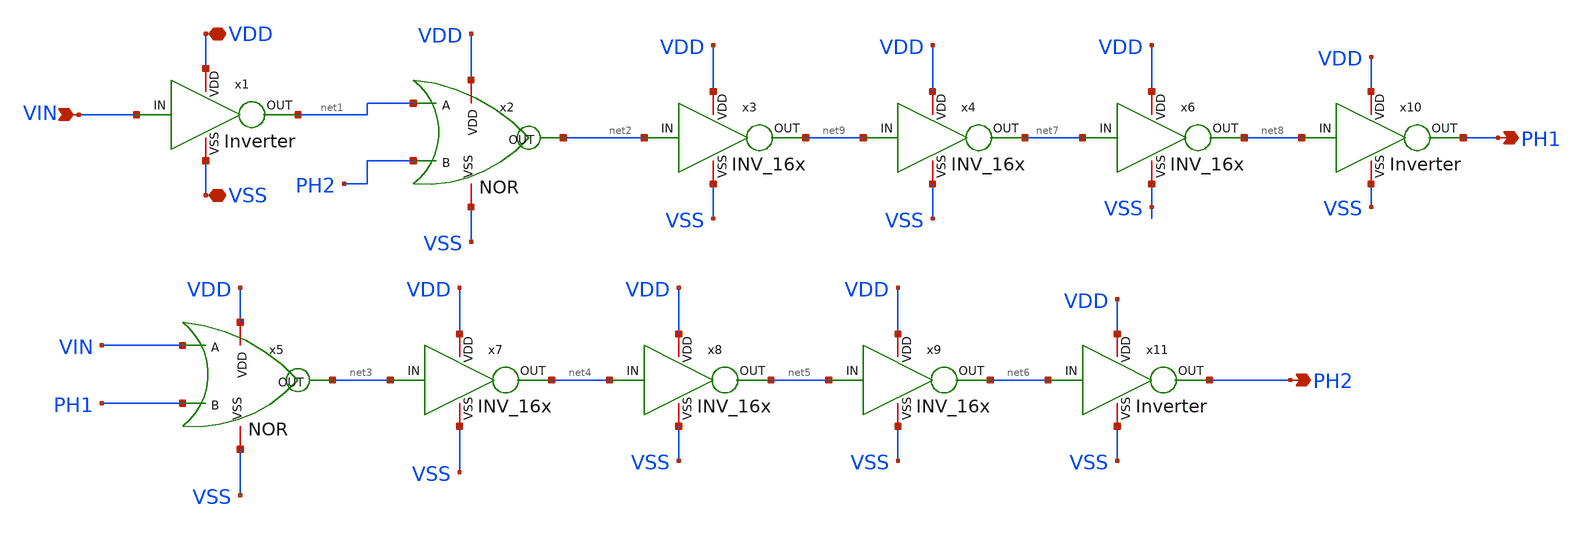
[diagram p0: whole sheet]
** sch_path: SCOP_INPUT_AND_MUX_PAKISTAN_03/Xschem/Non_OvL_CLK_Gen/Non_Overlapping_clk.sch
**.subckt Non_Overlapping_clk VDD VSS VIN PH1 PH2
*.iopin VDD
*.iopin VSS
*.ipin VIN
*.opin PH1
*.opin PH2
x1 VDD net1 VIN VSS Inverter
x10 VDD PH1 net8 VSS Inverter
x11 VDD PH2 net6 VSS Inverter
x3 VDD net9 net2 VSS INV_16x
x4 VDD net7 net9 VSS INV_16x
x6 VDD net8 net7 VSS INV_16x
x7 VDD net4 net3 VSS INV_16x
x8 VDD net5 net4 VSS INV_16x
x9 VDD net6 net5 VSS INV_16x
x2 VDD VSS net2 net1 PH2 NOR
x5 VDD VSS net3 VIN PH1 NOR
**.ends
.end
